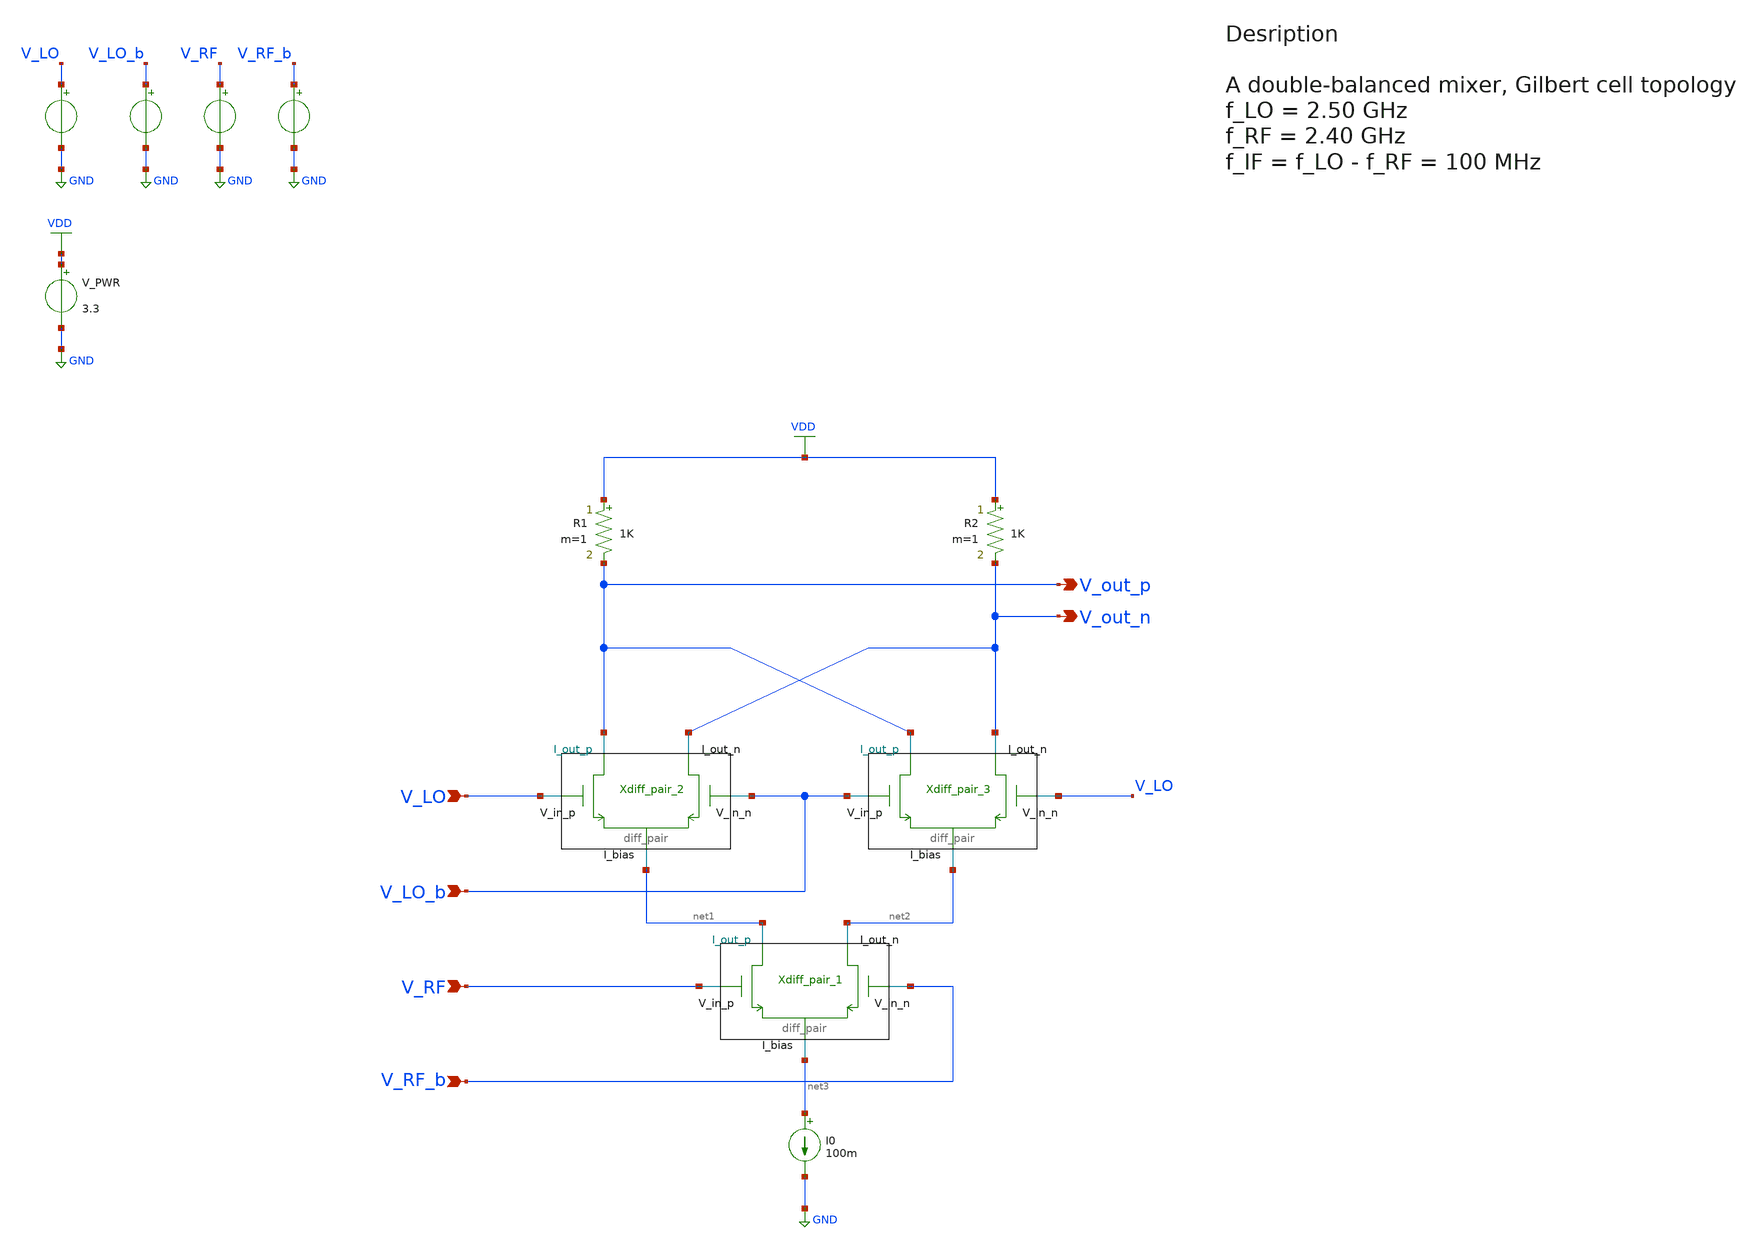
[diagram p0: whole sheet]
** sch_path: src/design_xsch/Gilbert_cell.sch
**.subckt Gilbert_cell V_LO V_LO_b V_RF V_RF_b V_out_p V_out_n
*.ipin V_LO
*.ipin V_LO_b
*.ipin V_RF
*.ipin V_RF_b
*.opin V_out_p
*.opin V_out_n
I0 net3 GND 100m
Xdiff_pair_1 net2 net1 V_RF V_RF_b net3 VSS diff_pair W_neg=0.22u L_neg=0.28u W_pos=2u L_pos=0.28u
+ m=1
Xdiff_pair_2 V_out_n V_out_p V_LO V_LO_b net1 VSS diff_pair W_neg=0.22u L_neg=0.28u W_pos=0.22u
+ L_pos=0.28u m=1
Xdiff_pair_3 V_out_n V_out_p V_LO_b V_LO net2 VSS diff_pair W_neg=0.22u L_neg=0.28u W_pos=0.22u
+ L_pos=0.28u m=1
R1 VDD V_out_p 1K m=1
R2 VDD V_out_n 1K m=1
V_PWR VDD GND 3.3
.save i(v_pwr)
VLO V_LO GND sin( cm_lo amp_lo freq_lo 0 )
.save i(vlo)
VLOb V_LO_b GND sin( cm_lo amp_lo freq_lo 0 0 180 )
.save i(vlob)
V_RF V_RF GND sin( cm_rf amp_rf freq_rf 0 )
.save i(v_rf)
V_RFb V_RF_b GND sin( cm_rf amp_rf freq_rf 0 0 180 )
.save i(v_rfb)
**** begin user architecture code

.include $::180MCU_MODELS/design.ngspice
.lib $::180MCU_MODELS/sm141064.ngspice typical




* parameters used in the voltage source, initialization
.param freq_lo=2.5e9 amp_lo=2 cm_lo=1.5 freq_rf=1e9 amp_rf=2 cm_rf=1

.control

    * Set frequency and amplitude parameters to proper values from within the control sequence
    alterparam cm_lo  = 0.7
    alterparam freq_lo = 2.50G
    alterparam amp_lo  = 0.2

    alterparam cm_rf  = 0.7
    alterparam freq_rf = 2.40G
    alterparam amp_rf  = 0.2
    reset

    let freq_if = abs( freq_lo - freq_rf )

    save all

    * operating point
    op
    write Gilbert_sim.raw

    set appendwrite

    * Transient analysis to observe mixing operation
    tran 1p 10n
    write Gilbert_sim.raw

    * Calculate differential output for conversion gain measurement
    let v_out_diff = v(v_out_p) - v(v_out_n)
    let v_rf_diff = v(v_rf) - v(v_rf_b)

    * Extract IF component at 100MHz using FFT
    linearize v_out_diff v_rf_diff
    let time_step = 10e-12
    let sample_freq = 1/time_step
    let npts = length(v_out_diff)
    let freq_res = sample_freq/npts
    print freq_res

    fft v_out_diff v_rf_diff

    * Find frequency bins
    print freq_if
    print freq_rf

    let if_bin = floor( freq_if / freq_res )
    let rf_bin = floor(freq_rf/freq_res)

    * Measure conversion gain (power gain from RF to IF)
    let rf_mag = abs(v_rf_diff[rf_bin])
    let if_mag = abs(v_out_diff[if_bin])
    let conversion_gain_db = 20*log10(if_mag/rf_mag)
    print conversion_gain_db

    * write Gilbert_cell.raw

.endc


**** end user architecture code
**.ends

* expanding   symbol:  /home/vasil/Downloads/SSCS_PICO_2025/src/design_xsch/diff_pair.sym # of
*+ pins=5
** sym_path: src/design_xsch/diff_pair.sym
** sch_path: src/design_xsch/diff_pair.sch
.subckt diff_pair I_out_n I_out_p V_in_p V_in_n I_bias VSSPIN  mult=1  W_neg=0.22u L_neg=0.28u
+ W_pos=0.22u L_pos=0.28u
*.ipin V_in_p
*.ipin V_in_n
*.iopin I_out_p
*.iopin I_out_n
*.iopin I_bias
XM1 I_out_p V_in_p I_bias VSS nfet_03v3 L=L_pos W=W_pos nf=1 ad='int((nf+1)/2) * W/nf * 0.18u' as='int((nf+2)/2) * W/nf * 0.18u'
+ pd='2*int((nf+1)/2) * (W/nf + 0.18u)' ps='2*int((nf+2)/2) * (W/nf + 0.18u)' nrd='0.18u / W' nrs='0.18u / W'
+ sa=0 sb=0 sd=0 m=mult
XM2 I_out_n V_in_n I_bias VSS nfet_03v3 L=L_neg W=W_neg nf=1 ad='int((nf+1)/2) * W/nf * 0.18u' as='int((nf+2)/2) * W/nf * 0.18u'
+ pd='2*int((nf+1)/2) * (W/nf + 0.18u)' ps='2*int((nf+2)/2) * (W/nf + 0.18u)' nrd='0.18u / W' nrs='0.18u / W'
+ sa=0 sb=0 sd=0 m=mult
.ends

.GLOBAL VDD
.GLOBAL GND
.GLOBAL VSS
.end
